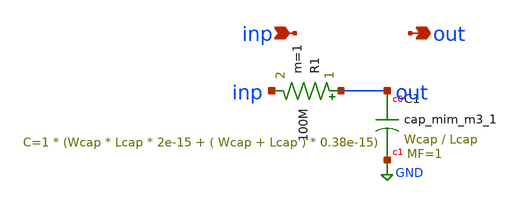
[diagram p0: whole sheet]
** sch_path: xschem/tryandtest/archive/RCPole.sch
**.subckt RCPole out inp
*.opin out
*.ipin inp
XC1 out GND sky130_fd_pr__cap_mim_m3_1 W=Wcap L=Lcap MF=1 m=1
R1 out inp 100M m=1
**.ends
.GLOBAL GND
.end
